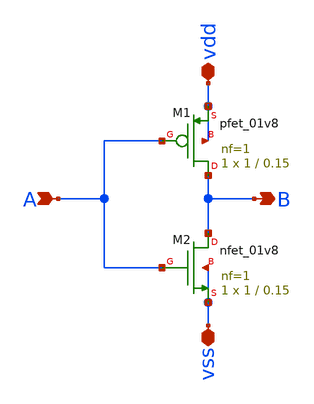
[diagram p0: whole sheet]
** sch_path: week0/netlists/xschem/inverter/schematics/inverter.sch
**.subckt inverter B A vdd vss
*.opin B
*.ipin A
*.iopin vdd
*.iopin vss
XM1 B A vdd vdd sky130_fd_pr__pfet_01v8 L=0.15 W=1 nf=1 ad='int((nf+1)/2) * W/nf * 0.29' as='int((nf+2)/2) * W/nf * 0.29'
+ pd='2*int((nf+1)/2) * (W/nf + 0.29)' ps='2*int((nf+2)/2) * (W/nf + 0.29)' nrd='0.29 / W' nrs='0.29 / W'
+ sa=0 sb=0 sd=0 mult=1 m=1
XM2 B A vss vss sky130_fd_pr__nfet_01v8 L=0.15 W=1 nf=1 ad='int((nf+1)/2) * W/nf * 0.29' as='int((nf+2)/2) * W/nf * 0.29'
+ pd='2*int((nf+1)/2) * (W/nf + 0.29)' ps='2*int((nf+2)/2) * (W/nf + 0.29)' nrd='0.29 / W' nrs='0.29 / W'
+ sa=0 sb=0 sd=0 mult=1 m=1
**.ends
.end
